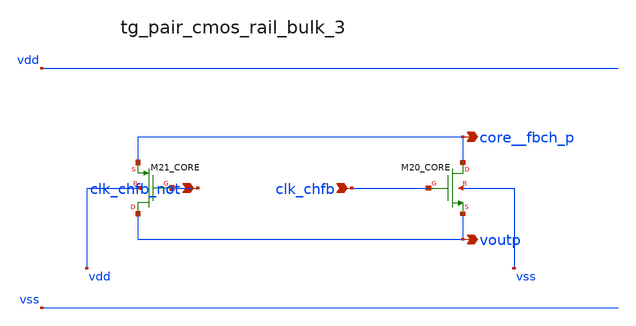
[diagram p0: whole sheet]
** sch_path: analog-db/raw/ia_006_fan_chopper_cmfb/hier/blocks/tg_pair_cmos_rail_bulk_3.sch
**.subckt tg_pair_cmos_rail_bulk_3 clk_chfb_not clk_chfb core__fbch_p voutp
*.ipin clk_chfb_not
*.ipin clk_chfb
*.opin core__fbch_p
*.opin voutp
XM20_CORE core__fbch_p clk_chfb voutp vss sg13_lv_nmos w=x_dut_xm20_core_w l=x_dut_xm20_core_l ng=1
+ m=x_dut_xm20_core_m
XM21_CORE voutp clk_chfb_not core__fbch_p vdd sg13_lv_pmos w=x_dut_xm21_core_w l=x_dut_xm21_core_l
+ ng=1 m=x_dut_xm21_core_m
**.ends
.end
